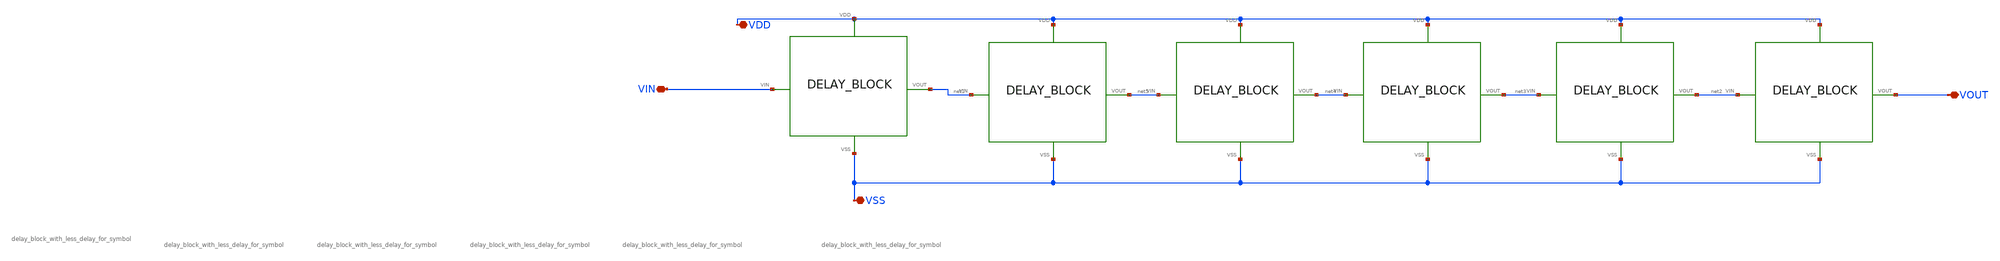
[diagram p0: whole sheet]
** sch_path: xschem/DC_DC_Converter_xschem/OTHERS/DC_DC_Converter_JV11/Delay_block_revised/delay_block_20.sch
**.subckt delay_block_20 VIN VDD VSS VOUT
*.iopin VIN
*.iopin VDD
*.iopin VSS
*.iopin VOUT
X1 VIN net1 VDD VSS delay_block_with_less_delay_for_symbol
X2 net1 net5 VDD VSS delay_block_with_less_delay_for_symbol
X3 net5 net4 VDD VSS delay_block_with_less_delay_for_symbol
X4 net4 net3 VDD VSS delay_block_with_less_delay_for_symbol
X5 net3 net2 VDD VSS delay_block_with_less_delay_for_symbol
X6 net2 VOUT VDD VSS delay_block_with_less_delay_for_symbol
**.ends
.end
